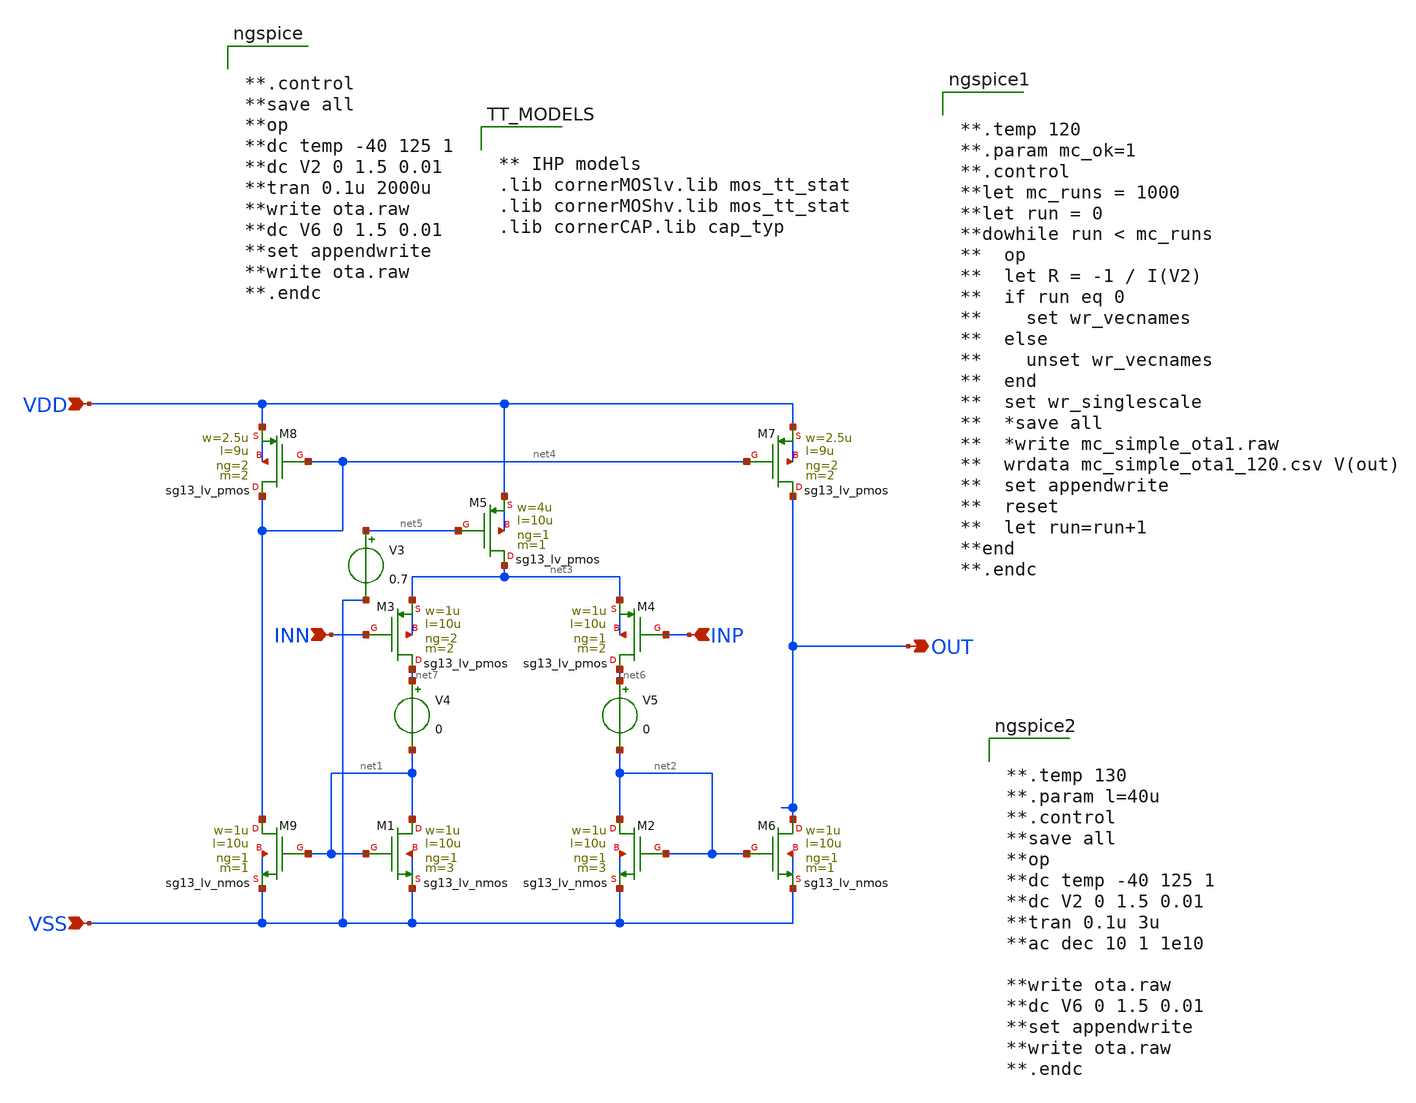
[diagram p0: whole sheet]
** sch_path: 10_xschem/ctat_ota.sch
**.subckt ctat_ota VDD VSS INN INP OUT
*.ipin VDD
*.ipin VSS
*.ipin INN
*.ipin INP
*.opin OUT
XM1 net1 net1 VSS VSS sg13_lv_nmos w=1u l=10u ng=1 m=3 mm_ok=1
XM3 net7 INN net3 net3 sg13_lv_pmos w=1u l=10u ng=2 m=2 mm_ok=1
XM4 net6 INP net3 net3 sg13_lv_pmos w=1u l=10u ng=1 m=2 mm_ok=1
XM2 net2 net2 VSS VSS sg13_lv_nmos w=1u l=10u ng=1 m=3 mm_ok=1
XM5 net3 net5 VDD VDD sg13_lv_pmos w=4u l=10u ng=1 m=1 mm_ok=1
XM6 OUT net2 VSS VSS sg13_lv_nmos w=1u l=10u ng=1 m=1 mm_ok=1
XM7 OUT net4 VDD VDD sg13_lv_pmos w=2.5u l=9u ng=2 m=2 mm_ok=1
XM8 net4 net4 VDD VDD sg13_lv_pmos w=2.5u l=9u ng=2 m=2 mm_ok=1
XM9 net4 net1 VSS VSS sg13_lv_nmos w=1u l=10u ng=1 m=1 mm_ok=1
V3 net5 VSS 0.7
V4 net7 net1 0
V5 net6 net2 0
**** begin user architecture code


**.control
**save all
**op
**dc temp -40 125 1
**dc V2 0 1.5 0.01
**tran 0.1u 2000u
**write ota.raw
**dc V6 0 1.5 0.01
**set appendwrite
**write ota.raw
**.endc




** IHP models
.lib cornerMOSlv.lib mos_tt_stat
.lib cornerMOShv.lib mos_tt_stat
.lib cornerCAP.lib cap_typ




**.temp 120
**.param mc_ok=1
**.control
**let mc_runs = 1000
**let run = 0
**dowhile run < mc_runs
**  op
**  let R = -1 / I(V2)
**  if run eq 0
**    set wr_vecnames
**  else
**    unset wr_vecnames
**  end
**  set wr_singlescale
**  *save all
**  *write mc_simple_ota1.raw
**  wrdata mc_simple_ota1_120.csv V(out)
**  set appendwrite
**  reset
**  let run=run+1
**end
**.endc




**.temp 130
**.param l=40u
**.control
**save all
**op
**dc temp -40 125 1
**dc V2 0 1.5 0.01
**tran 0.1u 3u
**ac dec 10 1 1e10

**write ota.raw
**dc V6 0 1.5 0.01
**set appendwrite
**write ota.raw
**.endc


**** end user architecture code
**.ends
.end
